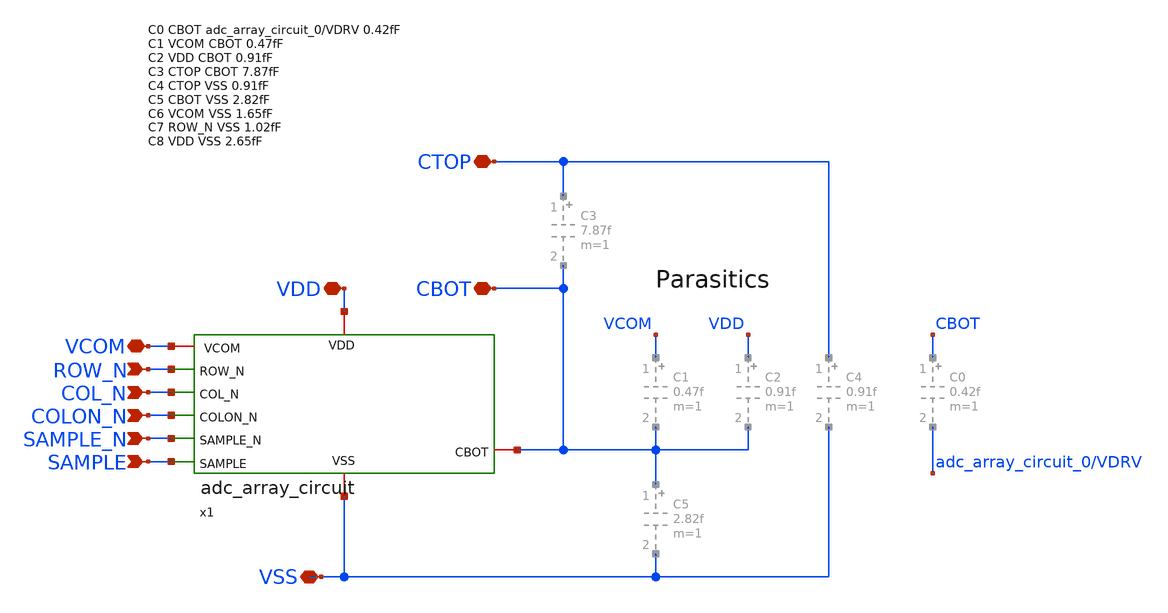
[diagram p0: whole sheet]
** sch_path: xschem/adc_array_cap/adc_array_cap_16.sch
**.subckt adc_array_cap_16 SAMPLE_N SAMPLE VCOM ROW_N COL_N COLON_N VDD CTOP VSS CBOT
*.ipin SAMPLE_N
*.ipin SAMPLE
*.iopin VCOM
*.ipin ROW_N
*.ipin COL_N
*.ipin COLON_N
*.iopin VDD
*.iopin CTOP
*.iopin VSS
*.iopin CBOT
x1 VDD ROW_N CBOT COL_N COLON_N SAMPLE_N VCOM SAMPLE VSS adc_array_circuit
**.ends

* expanding   symbol:  adc_array_circuit.sym # of pins=9
** sym_path: xschem/adc_array_cap/adc_array_circuit.sym
** sch_path: xschem/adc_array_cap/adc_array_circuit.sch
.subckt adc_array_circuit VDD ROW_N CBOT COL_N COLON_N SAMPLE_N VCOM SAMPLE VSS
*.ipin SAMPLE_N
*.ipin SAMPLE
*.iopin VCOM
*.ipin ROW_N
*.ipin COL_N
*.ipin COLON_N
*.iopin VDD
*.iopin VSS
*.iopin CBOT
XM1 VCOM SAMPLE CBOT VSS sky130_fd_pr__nfet_01v8 L=0.18 W=0.42 nf=1 ad='int((nf+1)/2) * W/nf * 0.29'
+ as='int((nf+2)/2) * W/nf * 0.29' pd='2*int((nf+1)/2) * (W/nf + 0.29)' ps='2*int((nf+2)/2) * (W/nf + 0.29)'
+ nrd='0.29 / W' nrs='0.29 / W' sa=0 sb=0 sd=0 mult=1 m=1
XM3 VCOM SAMPLE_N CBOT VDD sky130_fd_pr__pfet_01v8 L=0.18 W=0.9 nf=1 ad='int((nf+1)/2) * W/nf * 0.29'
+ as='int((nf+2)/2) * W/nf * 0.29' pd='2*int((nf+1)/2) * (W/nf + 0.29)' ps='2*int((nf+2)/2) * (W/nf + 0.29)'
+ nrd='0.29 / W' nrs='0.29 / W' sa=0 sb=0 sd=0 mult=1 m=1
XM2 VDRV SAMPLE_N CBOT VSS sky130_fd_pr__nfet_01v8 L=0.18 W=0.42 nf=1 ad='int((nf+1)/2) * W/nf * 0.29'
+ as='int((nf+2)/2) * W/nf * 0.29' pd='2*int((nf+1)/2) * (W/nf + 0.29)' ps='2*int((nf+2)/2) * (W/nf + 0.29)'
+ nrd='0.29 / W' nrs='0.29 / W' sa=0 sb=0 sd=0 mult=1 m=1
XM4 VDRV SAMPLE CBOT VDD sky130_fd_pr__pfet_01v8 L=0.18 W=0.9 nf=1 ad='int((nf+1)/2) * W/nf * 0.29' as='int((nf+2)/2) * W/nf * 0.29'
+ pd='2*int((nf+1)/2) * (W/nf + 0.29)' ps='2*int((nf+2)/2) * (W/nf + 0.29)' nrd='0.29 / W' nrs='0.29 / W'
+ sa=0 sb=0 sd=0 mult=1 m=1
XM5 VINT1 COL_N VDRV VDD sky130_fd_pr__pfet_01v8 L=0.18 W=0.9 nf=1 ad='int((nf+1)/2) * W/nf * 0.29' as='int((nf+2)/2) * W/nf * 0.29'
+ pd='2*int((nf+1)/2) * (W/nf + 0.29)' ps='2*int((nf+2)/2) * (W/nf + 0.29)' nrd='0.29 / W' nrs='0.29 / W'
+ sa=0 sb=0 sd=0 mult=1 m=1
XM6 VDD ROW_N VINT1 VDD sky130_fd_pr__pfet_01v8 L=0.18 W=0.9 nf=1 ad='int((nf+1)/2) * W/nf * 0.29' as='int((nf+2)/2) * W/nf * 0.29'
+ pd='2*int((nf+1)/2) * (W/nf + 0.29)' ps='2*int((nf+2)/2) * (W/nf + 0.29)' nrd='0.29 / W' nrs='0.29 / W'
+ sa=0 sb=0 sd=0 mult=1 m=1
XM7 VDD COLON_N VDRV VDD sky130_fd_pr__pfet_01v8 L=0.18 W=0.9 nf=1 ad='int((nf+1)/2) * W/nf * 0.29' as='int((nf+2)/2) * W/nf * 0.29'
+ pd='2*int((nf+1)/2) * (W/nf + 0.29)' ps='2*int((nf+2)/2) * (W/nf + 0.29)' nrd='0.29 / W' nrs='0.29 / W'
+ sa=0 sb=0 sd=0 mult=1 m=1
XM8 VINT2 COLON_N VDRV VSS sky130_fd_pr__nfet_01v8 L=0.18 W=0.42 nf=1 ad='int((nf+1)/2) * W/nf * 0.29'
+ as='int((nf+2)/2) * W/nf * 0.29' pd='2*int((nf+1)/2) * (W/nf + 0.29)' ps='2*int((nf+2)/2) * (W/nf + 0.29)'
+ nrd='0.29 / W' nrs='0.29 / W' sa=0 sb=0 sd=0 mult=1 m=1
XM9 VSS ROW_N VINT2 VSS sky130_fd_pr__nfet_01v8 L=0.18 W=0.42 nf=1 ad='int((nf+1)/2) * W/nf * 0.29' as='int((nf+2)/2) * W/nf * 0.29'
+ pd='2*int((nf+1)/2) * (W/nf + 0.29)' ps='2*int((nf+2)/2) * (W/nf + 0.29)' nrd='0.29 / W' nrs='0.29 / W'
+ sa=0 sb=0 sd=0 mult=1 m=1
XM10 VSS COL_N VINT2 VSS sky130_fd_pr__nfet_01v8 L=0.18 W=0.42 nf=1 ad='int((nf+1)/2) * W/nf * 0.29'
+ as='int((nf+2)/2) * W/nf * 0.29' pd='2*int((nf+1)/2) * (W/nf + 0.29)' ps='2*int((nf+2)/2) * (W/nf + 0.29)'
+ nrd='0.29 / W' nrs='0.29 / W' sa=0 sb=0 sd=0 mult=1 m=1
.ends

.end
